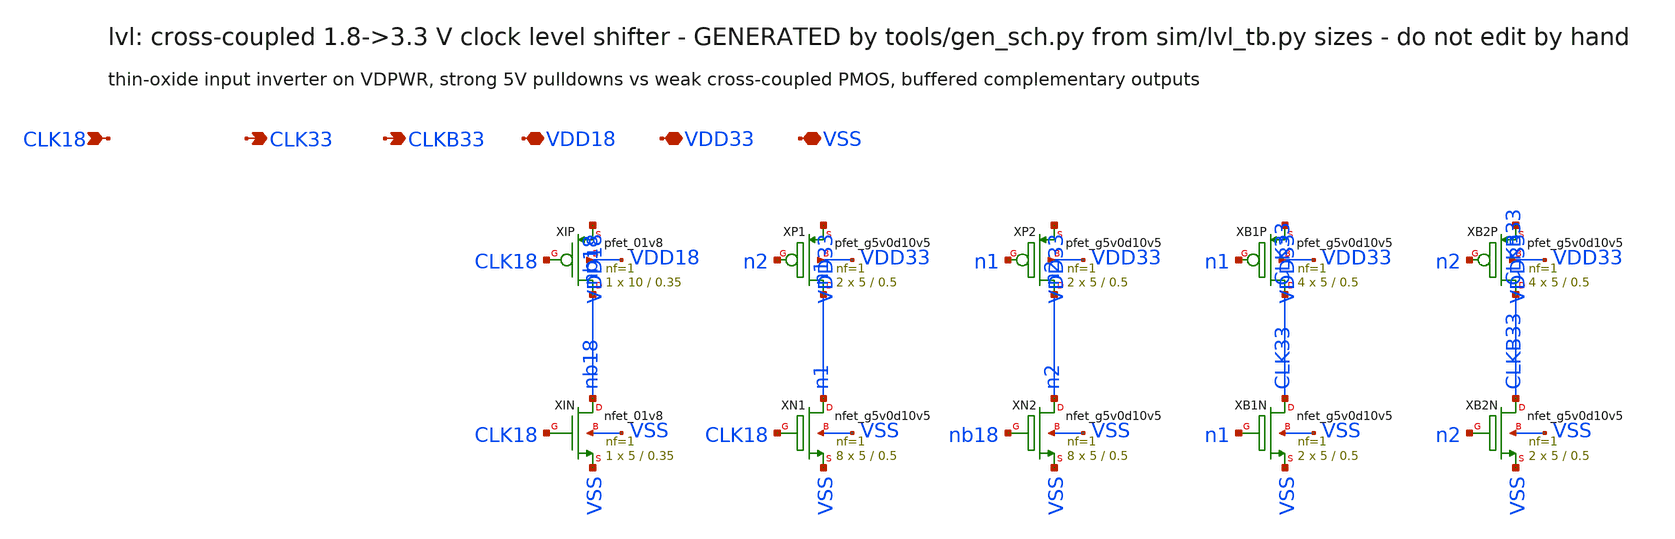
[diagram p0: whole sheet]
** sch_path: xschem/lvl.sch
**.subckt lvl CLK18 CLK33 CLKB33 VDD18 VDD33 VSS
*.ipin CLK18
*.opin CLK33
*.opin CLKB33
*.iopin VDD18
*.iopin VDD33
*.iopin VSS
XXIP nb18 CLK18 VDD18 VDD18 sky130_fd_pr__pfet_01v8 L=0.35 W=10 nf=1 ad=0 as=0 pd=0 ps=0 nrd=0 nrs=0
+ sa=0 sb=0 sd=0 mult=1 m=1
XXIN nb18 CLK18 VSS VSS sky130_fd_pr__nfet_01v8 L=0.35 W=5 nf=1 ad=0 as=0 pd=0 ps=0 nrd=0 nrs=0 sa=0
+ sb=0 sd=0 mult=1 m=1
XXP1 n1 n2 VDD33 VDD33 sky130_fd_pr__pfet_g5v0d10v5 L=0.5 W=5 nf=1 ad=0 as=0 pd=0 ps=0 nrd=0 nrs=0
+ sa=0 sb=0 sd=0 mult=2 m=2
XXP2 n2 n1 VDD33 VDD33 sky130_fd_pr__pfet_g5v0d10v5 L=0.5 W=5 nf=1 ad=0 as=0 pd=0 ps=0 nrd=0 nrs=0
+ sa=0 sb=0 sd=0 mult=2 m=2
XXN1 n1 CLK18 VSS VSS sky130_fd_pr__nfet_g5v0d10v5 L=0.5 W=5 nf=1 ad=0 as=0 pd=0 ps=0 nrd=0 nrs=0
+ sa=0 sb=0 sd=0 mult=8 m=8
XXN2 n2 nb18 VSS VSS sky130_fd_pr__nfet_g5v0d10v5 L=0.5 W=5 nf=1 ad=0 as=0 pd=0 ps=0 nrd=0 nrs=0
+ sa=0 sb=0 sd=0 mult=8 m=8
XXB1P CLK33 n1 VDD33 VDD33 sky130_fd_pr__pfet_g5v0d10v5 L=0.5 W=5 nf=1 ad=0 as=0 pd=0 ps=0 nrd=0
+ nrs=0 sa=0 sb=0 sd=0 mult=4 m=4
XXB1N CLK33 n1 VSS VSS sky130_fd_pr__nfet_g5v0d10v5 L=0.5 W=5 nf=1 ad=0 as=0 pd=0 ps=0 nrd=0 nrs=0
+ sa=0 sb=0 sd=0 mult=2 m=2
XXB2P CLKB33 n2 VDD33 VDD33 sky130_fd_pr__pfet_g5v0d10v5 L=0.5 W=5 nf=1 ad=0 as=0 pd=0 ps=0 nrd=0
+ nrs=0 sa=0 sb=0 sd=0 mult=4 m=4
XXB2N CLKB33 n2 VSS VSS sky130_fd_pr__nfet_g5v0d10v5 L=0.5 W=5 nf=1 ad=0 as=0 pd=0 ps=0 nrd=0 nrs=0
+ sa=0 sb=0 sd=0 mult=2 m=2
**.ends
.end
